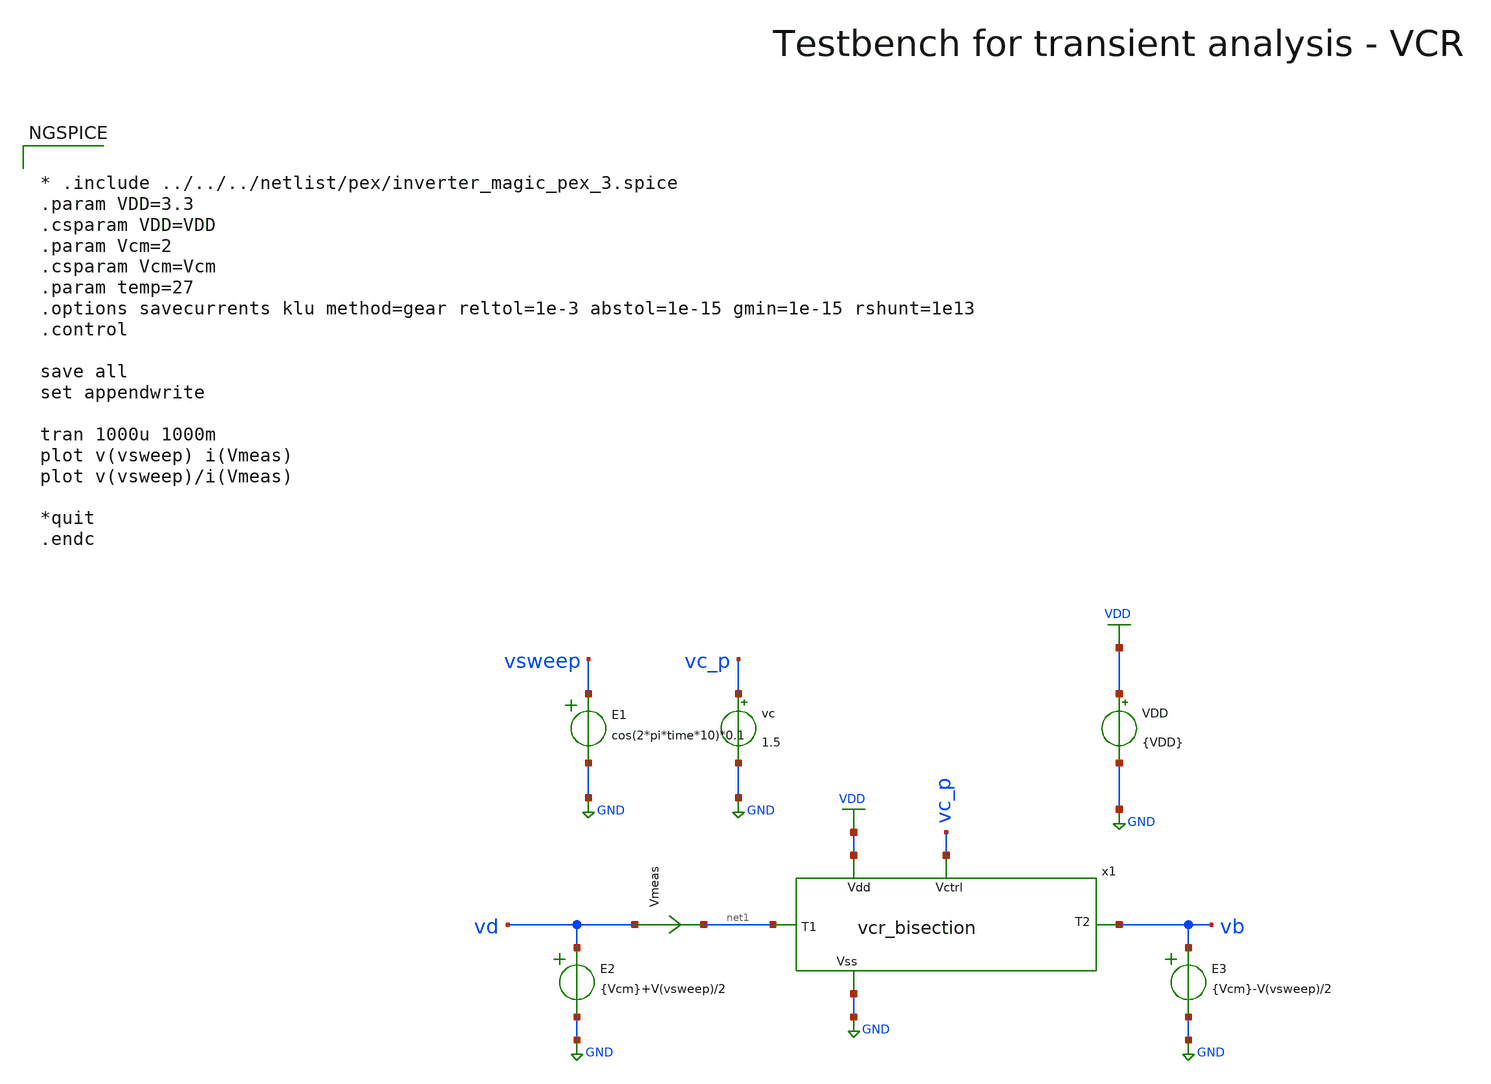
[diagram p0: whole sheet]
** sch_path: macros/voltage_controlled_resistors/macros/vcr_bisection/testbenches/xschem/res_tb_tran.sch
**.subckt res_tb_tran
VDD VDD GND {VDD}
Vmeas vd net1 0
.save i(vmeas)
E2 vd GND VOL=' {Vcm}+V(vsweep)/2 '
E3 vb GND VOL=' {Vcm}-V(vsweep)/2 '
vc vc_p GND 1.5
x1 vc_p net1 vb VDD GND vcr_bisection
E1 vsweep GND VOL=' cos(2*pi*time*10)*0.1 '
**** begin user architecture code

.lib cornerMOSlv.lib mos_tt
.lib cornerMOShv.lib mos_tt
.lib cornerRES.lib res_typ
.lib cornerDIO.lib dio_tt



* .include ../../../netlist/pex/inverter_magic_pex_3.spice
.param VDD=3.3
.csparam VDD=VDD
.param Vcm=2
.csparam Vcm=Vcm
.param temp=27
.options savecurrents klu method=gear reltol=1e-3 abstol=1e-15 gmin=1e-15 rshunt=1e13
.control

save all
set appendwrite

tran 1000u 1000m
plot v(vsweep) i(Vmeas)
plot v(vsweep)/i(Vmeas)

*quit
.endc


**** end user architecture code
**.ends
.GLOBAL GND
.GLOBAL VDD
.end
